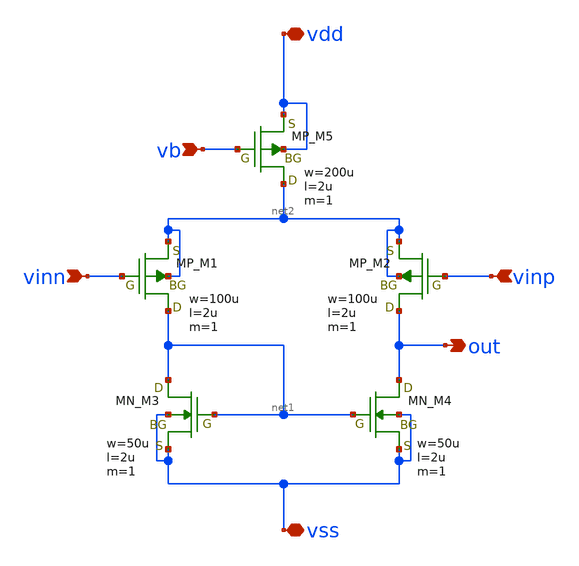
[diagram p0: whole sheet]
** sch_path: member_project/opamp/makoto645/diff.sch
**.subckt diff vinn vinp vb out vdd vss
*.ipin vinn
*.ipin vinp
*.ipin vb
*.opin out
*.iopin vdd
*.iopin vss
XM5 net2 vb vdd vdd PMOS w=200u l=2u as=0 ad=0 ps=0 pd=0 nrd=0 nrs=0 m=1
XM1 net1 vinn net2 net2 PMOS w=100u l=2u as=0 ad=0 ps=0 pd=0 nrd=0 nrs=0 m=1
XM2 out vinp net2 net2 PMOS w=100u l=2u as=0 ad=0 ps=0 pd=0 nrd=0 nrs=0 m=1
XM3 net1 net1 vss vss NMOS w=50u l=2u as=0 ad=0 ps=0 pd=0 nrd=0 nrs=0 m=1
XM4 out net1 vss vss NMOS w=50u l=2u as=0 ad=0 ps=0 pd=0 nrd=0 nrs=0 m=1
**.ends
.end
